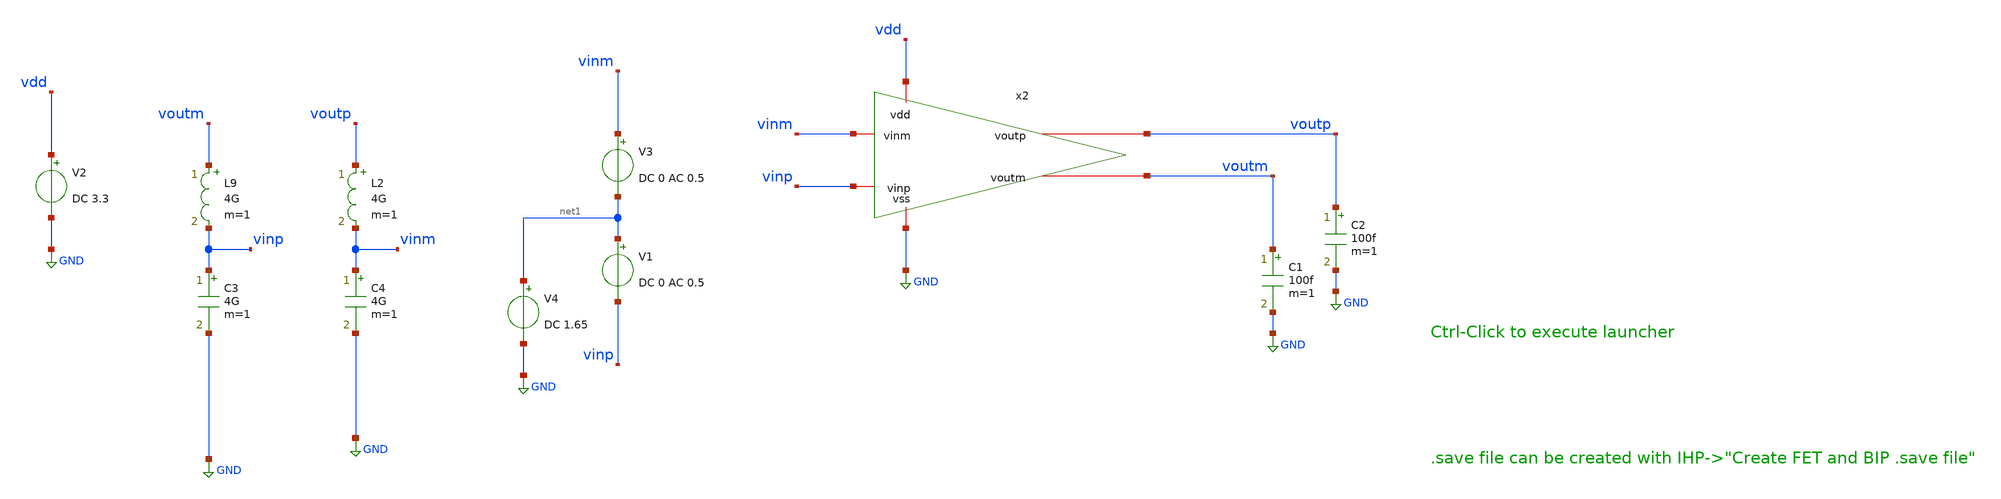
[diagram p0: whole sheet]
** sch_path: testbench/aux_amp_tb.sch
**.subckt aux_amp_tb
C2 voutp GND 100f m=1
V2 vdd GND DC 3.3
L9 voutm vinp 4G m=1
C3 vinp GND 4G m=1
x2 vdd vinm vinp voutp voutm GND aux_amp
C1 voutm GND 100f m=1
L2 voutp vinm 4G m=1
C4 vinm GND 4G m=1
V1 net1 vinp DC 0 AC 0.5
V3 vinm net1 DC 0 AC 0.5
V4 net1 GND DC 1.65
**** begin user architecture code

.lib cornerMOShv.lib mos_tt
.lib $::SG13G2_MODELS/cornerCAP.lib cap_typ



.param temp=27
.include aux_amp_tb.save
.control

* --- OP ---
op
save all
write aux_amp_tb.raw
set appendwrite

* --- DC Sweep ---
tran 10u 10m
save all

* --- AC Sweep ---
ac dec 100 1 100e6
save all

let Av = db(v(voutp))
let phase = 180/3.14*vp(voutp) + 180
let CMRR = db((v(voutp)/v(vinp))/(v(voutp_cmrr)/v(vinp)))
let PSRR = db(v(voutp_psrr)/v(vdd_ac))

echo ---
meas ac gm_db find vdb(voutp) when vp(voutp)=0
meas ac pm_deg find phase when vdb(voutp)=0
meas ac _3db_f when phase=-45
meas ac _0db_f when vdb(voutp)=0
meas ac dc_gain find vdb(voutp) at=1
echo ---

write aux_amp_tb.raw
.endc


**** end user architecture code
**.ends

* expanding   symbol:  aux_amp.sym # of pins=6
** sym_path: schematic/aux_amp.sym
** sch_path: schematic/aux_amp.sch
.subckt aux_amp vdd vinm vinp voutp voutm vss
*.iopin vss
*.iopin voutm
*.iopin vinp
*.iopin vdd
*.iopin voutp
*.iopin vinm
XM1 net3 vinp net1 net1 sg13_hv_nmos w=80.0u l=10.0u ng=8 m=1 mm_ok=1
XM2 net4 cm_bias net1 net1 sg13_hv_nmos w=80.0u l=10.0u ng=8 m=1 mm_ok=1
XM5 net1 nbias vss vss sg13_hv_nmos w=29.0u l=10.0u ng=8 m=1 mm_ok=1
XM3 net3 cm_bias net2 net2 sg13_hv_nmos w=80.0u l=10.0u ng=8 m=1 mm_ok=1
XM4 net4 vinm net2 net2 sg13_hv_nmos w=80.0u l=10.0u ng=8 m=1 mm_ok=1
XM6 net2 nbias vss vss sg13_hv_nmos w=29.0u l=10.0u ng=8 m=1 mm_ok=1
XM11 voutm nbias vss vss sg13_hv_nmos w=29.0u l=10.0u ng=8 m=1 mm_ok=1
XM12 voutp nbias vss vss sg13_hv_nmos w=29.0u l=10.0u ng=8 m=1 mm_ok=1
V3 pbias vss 1.80
V4 cm_bias vss 1.65
XM9 voutm pbias net3 net3 sg13_hv_pmos w=15.0u l=2.0u ng=8 m=1 mm_ok=1
XM7 net3 pbias_top vdd vdd sg13_hv_pmos w=4.0u l=1.0u ng=1 m=1 mm_ok=1
XM8 net4 pbias_top vdd vdd sg13_hv_pmos w=4.0u l=1.0u ng=1 m=1 mm_ok=1
XM10 voutp pbias net4 net4 sg13_hv_pmos w=15.0u l=2.0u ng=8 m=1 mm_ok=1
XM14 nbias nbias vss vss sg13_hv_nmos w=29.0u l=10.0u ng=8 m=1 mm_ok=1
I1 vdd nbias 1.0u
V1 pbias_top vss 2.2
.ends

.GLOBAL GND
.end
